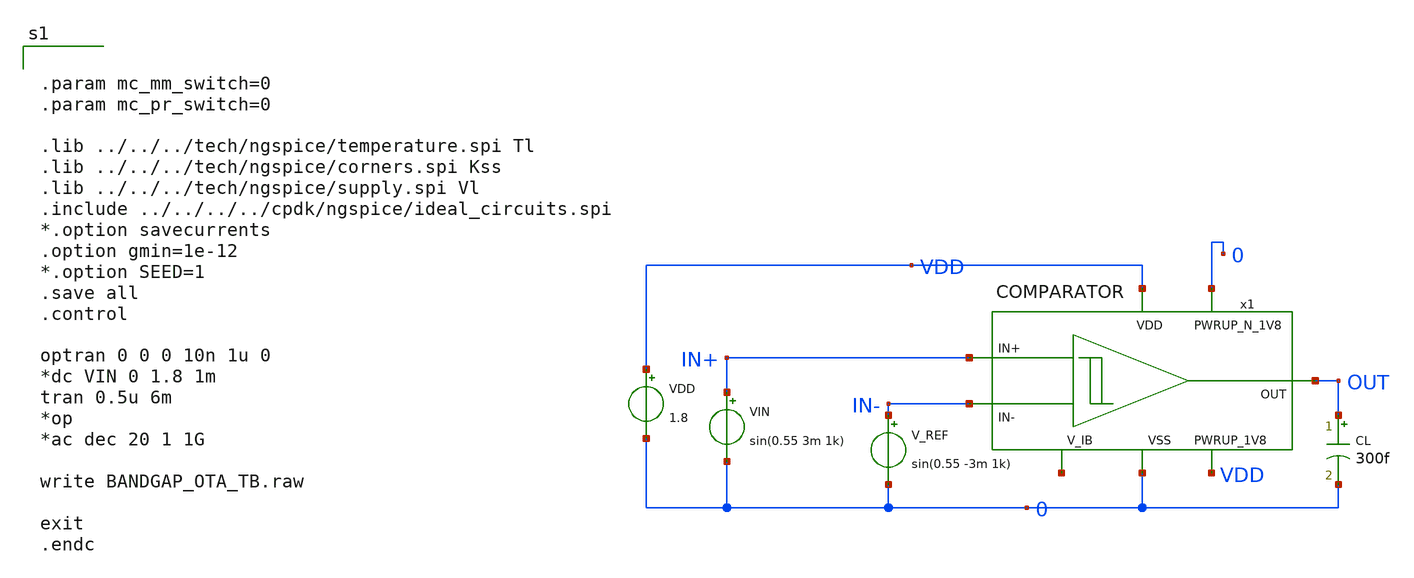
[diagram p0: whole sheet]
** sch_path: design/LELO_GR03_SKY130A/BANDGAP_OTA_TB.sch
**.subckt BANDGAP_OTA_TB
CL OUT 0 300f m=1
VIN IN+ 0 sin(0.55 3m 1k)
V_REF IN- 0 sin(0.55 -3m 1k)
VDD VDD 0 1.8
x1 VDD IN+ OUT IN- 0 0 VDD net1 COMPARATOR
**** begin user architecture code


.param mc_mm_switch=0
.param mc_pr_switch=0

.lib ../../../tech/ngspice/temperature.spi Tl
.lib ../../../tech/ngspice/corners.spi Kss
.lib ../../../tech/ngspice/supply.spi Vl
.include ../../../../cpdk/ngspice/ideal_circuits.spi
*.option savecurrents
.option gmin=1e-12
*.option SEED=1
.save all
.control

optran 0 0 0 10n 1u 0
*dc VIN 0 1.8 1m
tran 0.5u 6m
*op
*ac dec 20 1 1G

write BANDGAP_OTA_TB.raw

exit
.endc


**** end user architecture code
**.ends
.end
